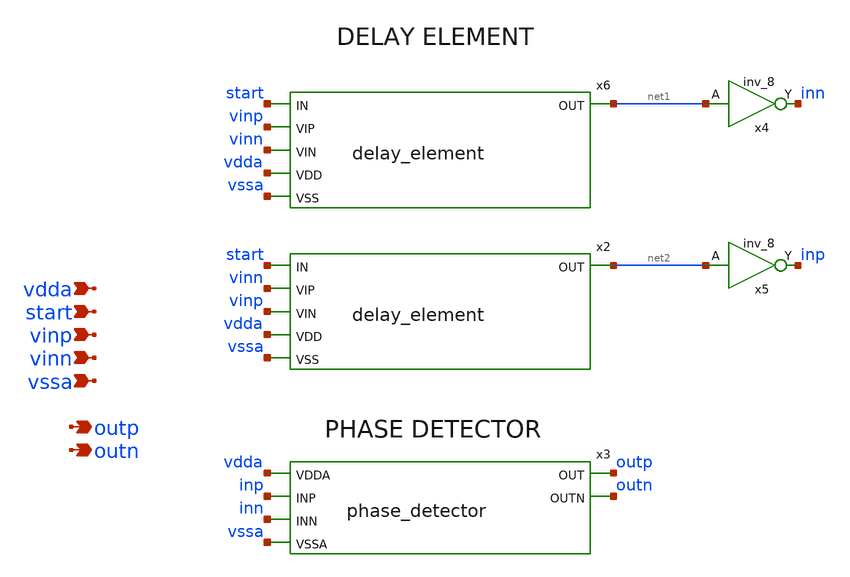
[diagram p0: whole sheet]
** sch_path: top/tdc.sch
**.subckt tdc vinn vinp vdda vssa start outp outn
*.ipin vinn
*.ipin vinp
*.ipin vdda
*.ipin vssa
*.ipin start
*.opin outp
*.opin outn
x4 net1 vssa vssa vdda vdda inn sky130_fd_sc_hd__inv_8
x5 net2 vssa vssa vdda vdda inp sky130_fd_sc_hd__inv_8
x6 start net1 vinp vinn vdda vssa delay_element
x2 start net2 vinn vinp vdda vssa delay_element
x3 vdda inp inn vssa outp outn phase_detector
**.ends

* expanding   symbol:  /foss/designs/delay_element.sym # of pins=6
** sym_path: top/delay_element.sym
** sch_path: top/delay_element.sch
.subckt delay_element IN OUT VIP VIN VDD VSS
*.ipin VDD
*.ipin VIN
*.ipin IN
*.ipin VSS
*.opin OUT
*.ipin VIP
XM1 net2 VIP VDD VDD sky130_fd_pr__pfet_01v8_lvt L=15 W=6 nf=1 ad='int((nf+1)/2) * W/nf * 0.29' as='int((nf+2)/2) * W/nf * 0.29'
+ pd='2*int((nf+1)/2) * (W/nf + 0.29)' ps='2*int((nf+2)/2) * (W/nf + 0.29)' nrd='0.29 / W' nrs='0.29 / W'
+ sa=0 sb=0 sd=0 mult=1 m=1
XM2 net1 IN net2 VDD sky130_fd_pr__pfet_01v8_lvt L=15 W=6 nf=1 ad='int((nf+1)/2) * W/nf * 0.29' as='int((nf+2)/2) * W/nf * 0.29'
+ pd='2*int((nf+1)/2) * (W/nf + 0.29)' ps='2*int((nf+2)/2) * (W/nf + 0.29)' nrd='0.29 / W' nrs='0.29 / W'
+ sa=0 sb=0 sd=0 mult=1 m=1
XM3 net1 IN VSS VSS sky130_fd_pr__nfet_01v8_lvt L=15 W=2 nf=1 ad='int((nf+1)/2) * W/nf * 0.29' as='int((nf+2)/2) * W/nf * 0.29'
+ pd='2*int((nf+1)/2) * (W/nf + 0.29)' ps='2*int((nf+2)/2) * (W/nf + 0.29)' nrd='0.29 / W' nrs='0.29 / W'
+ sa=0 sb=0 sd=0 mult=1 m=1
XM6 OUT net1 VDD VDD sky130_fd_pr__pfet_01v8_lvt L=15 W=6 nf=1 ad='int((nf+1)/2) * W/nf * 0.29' as='int((nf+2)/2) * W/nf * 0.29'
+ pd='2*int((nf+1)/2) * (W/nf + 0.29)' ps='2*int((nf+2)/2) * (W/nf + 0.29)' nrd='0.29 / W' nrs='0.29 / W'
+ sa=0 sb=0 sd=0 mult=1 m=1
XM7 OUT net1 net3 VSS sky130_fd_pr__nfet_01v8_lvt L=15 W=2 nf=1 ad='int((nf+1)/2) * W/nf * 0.29' as='int((nf+2)/2) * W/nf * 0.29'
+ pd='2*int((nf+1)/2) * (W/nf + 0.29)' ps='2*int((nf+2)/2) * (W/nf + 0.29)' nrd='0.29 / W' nrs='0.29 / W'
+ sa=0 sb=0 sd=0 mult=1 m=1
XM8 net3 VIN VSS VSS sky130_fd_pr__nfet_01v8_lvt L=15 W=2 nf=1 ad='int((nf+1)/2) * W/nf * 0.29' as='int((nf+2)/2) * W/nf * 0.29'
+ pd='2*int((nf+1)/2) * (W/nf + 0.29)' ps='2*int((nf+2)/2) * (W/nf + 0.29)' nrd='0.29 / W' nrs='0.29 / W'
+ sa=0 sb=0 sd=0 mult=1 m=1
.ends


* expanding   symbol:  /foss/designs/phase_detector.sym # of pins=6
** sym_path: top/phase_detector.sym
** sch_path: top/phase_detector.sch
.subckt phase_detector VDDA INP INN VSSA OUT OUTN
*.ipin VDDA
*.ipin INP
*.ipin INN
*.ipin VSSA
*.opin OUT
*.opin OUTN
x1 OUTN net3 VSSA VSSA VDDA VDDA OUT sky130_fd_sc_hd__nand2_1
x2 net5 OUT VSSA VSSA VDDA VDDA OUTN sky130_fd_sc_hd__nand2_1
XM1 net1 INN VDDA VDDA sky130_fd_pr__pfet_01v8 L=0.15 W=1 nf=1 ad='int((nf+1)/2) * W/nf * 0.29' as='int((nf+2)/2) * W/nf * 0.29'
+ pd='2*int((nf+1)/2) * (W/nf + 0.29)' ps='2*int((nf+2)/2) * (W/nf + 0.29)' nrd='0.29 / W' nrs='0.29 / W'
+ sa=0 sb=0 sd=0 mult=1 m=1
XM2 net3 INP net1 VDDA sky130_fd_pr__pfet_01v8 L=0.15 W=1 nf=1 ad='int((nf+1)/2) * W/nf * 0.29' as='int((nf+2)/2) * W/nf * 0.29'
+ pd='2*int((nf+1)/2) * (W/nf + 0.29)' ps='2*int((nf+2)/2) * (W/nf + 0.29)' nrd='0.29 / W' nrs='0.29 / W'
+ sa=0 sb=0 sd=0 mult=1 m=1
XM3 net2 INP VDDA VDDA sky130_fd_pr__pfet_01v8 L=0.15 W=1 nf=1 ad='int((nf+1)/2) * W/nf * 0.29' as='int((nf+2)/2) * W/nf * 0.29'
+ pd='2*int((nf+1)/2) * (W/nf + 0.29)' ps='2*int((nf+2)/2) * (W/nf + 0.29)' nrd='0.29 / W' nrs='0.29 / W'
+ sa=0 sb=0 sd=0 mult=1 m=1
XM4 net5 INN net2 VDDA sky130_fd_pr__pfet_01v8 L=0.15 W=1 nf=1 ad='int((nf+1)/2) * W/nf * 0.29' as='int((nf+2)/2) * W/nf * 0.29'
+ pd='2*int((nf+1)/2) * (W/nf + 0.29)' ps='2*int((nf+2)/2) * (W/nf + 0.29)' nrd='0.29 / W' nrs='0.29 / W'
+ sa=0 sb=0 sd=0 mult=1 m=1
XM5 net3 net5 VDDA VDDA sky130_fd_pr__pfet_01v8 L=0.15 W=1 nf=1 ad='int((nf+1)/2) * W/nf * 0.29' as='int((nf+2)/2) * W/nf * 0.29'
+ pd='2*int((nf+1)/2) * (W/nf + 0.29)' ps='2*int((nf+2)/2) * (W/nf + 0.29)' nrd='0.29 / W' nrs='0.29 / W'
+ sa=0 sb=0 sd=0 mult=1 m=1
XM6 net3 net5 net4 VSSA sky130_fd_pr__nfet_01v8 L=0.15 W=0.5 nf=1 ad='int((nf+1)/2) * W/nf * 0.29' as='int((nf+2)/2) * W/nf * 0.29'
+ pd='2*int((nf+1)/2) * (W/nf + 0.29)' ps='2*int((nf+2)/2) * (W/nf + 0.29)' nrd='0.29 / W' nrs='0.29 / W'
+ sa=0 sb=0 sd=0 mult=1 m=1
XM7 net4 INP VSSA VSSA sky130_fd_pr__nfet_01v8 L=0.15 W=0.5 nf=1 ad='int((nf+1)/2) * W/nf * 0.29' as='int((nf+2)/2) * W/nf * 0.29'
+ pd='2*int((nf+1)/2) * (W/nf + 0.29)' ps='2*int((nf+2)/2) * (W/nf + 0.29)' nrd='0.29 / W' nrs='0.29 / W'
+ sa=0 sb=0 sd=0 mult=1 m=1
XM8 net5 net3 VDDA VDDA sky130_fd_pr__pfet_01v8 L=0.15 W=1 nf=1 ad='int((nf+1)/2) * W/nf * 0.29' as='int((nf+2)/2) * W/nf * 0.29'
+ pd='2*int((nf+1)/2) * (W/nf + 0.29)' ps='2*int((nf+2)/2) * (W/nf + 0.29)' nrd='0.29 / W' nrs='0.29 / W'
+ sa=0 sb=0 sd=0 mult=1 m=1
XM9 net5 net3 net6 VSSA sky130_fd_pr__nfet_01v8 L=0.15 W=0.5 nf=1 ad='int((nf+1)/2) * W/nf * 0.29' as='int((nf+2)/2) * W/nf * 0.29'
+ pd='2*int((nf+1)/2) * (W/nf + 0.29)' ps='2*int((nf+2)/2) * (W/nf + 0.29)' nrd='0.29 / W' nrs='0.29 / W'
+ sa=0 sb=0 sd=0 mult=1 m=1
XM10 net6 INN VSSA VSSA sky130_fd_pr__nfet_01v8 L=0.15 W=0.5 nf=1 ad='int((nf+1)/2) * W/nf * 0.29' as='int((nf+2)/2) * W/nf * 0.29'
+ pd='2*int((nf+1)/2) * (W/nf + 0.29)' ps='2*int((nf+2)/2) * (W/nf + 0.29)' nrd='0.29 / W' nrs='0.29 / W'
+ sa=0 sb=0 sd=0 mult=1 m=1
.ends

.end
